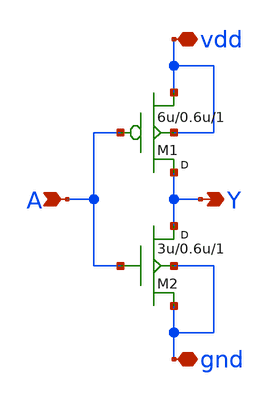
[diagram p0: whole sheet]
** sch_path: lab7/sch/made/INVx.sch
**.subckt INVx A Y vdd gnd
*.ipin A
*.opin Y
*.iopin vdd
*.iopin gnd
M1 Y A vdd vdd pfet w=6u l=0.6u m=1
M2 Y A gnd gnd nfet w=3u l=0.6u m=1
**.ends
.end
